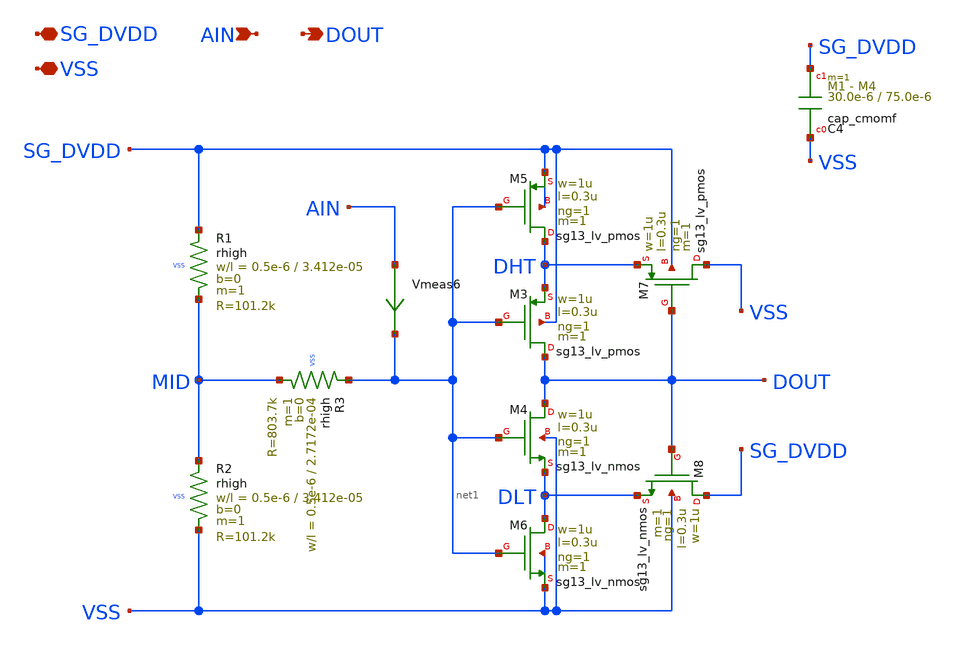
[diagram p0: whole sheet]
** sch_path: macros/schmitt_trigger_pullmid/schematic/xschem/schmitt_trigger_pullmid.sch
**.subckt schmitt_trigger_pullmid SG_DVDD VSS AIN DOUT
*.iopin SG_DVDD
*.iopin VSS
*.ipin AIN
*.opin DOUT
Vmeas6 AIN net1 0
.save i(vmeas6)
XR1 SG_DVDD MID VSS rhigh w=0.5e-6 l=3.412e-05 m=1 b=0 mm_ok=1
XR2 MID VSS VSS rhigh w=0.5e-6 l=3.412e-05 m=1 b=0 mm_ok=1
XR3 net1 MID VSS rhigh w=0.5e-6 l=2.7172e-04 m=1 b=0 mm_ok=1
XC4 VSS SG_DVDD cap_cmomf w=30.0e-6 l=75.0e-6 mmin=1 mmax=4 subblock=0 rfmodel=0 subscale=1 m=1
+ mm_ok=1
XM4 DOUT net1 DLT VSS sg13_lv_nmos w=1u l=0.3u ng=1 m=1 mm_ok=1
XM5 DHT net1 SG_DVDD SG_DVDD sg13_lv_pmos w=1u l=0.3u ng=1 m=1 mm_ok=1
XM3 DOUT net1 DHT SG_DVDD sg13_lv_pmos w=1u l=0.3u ng=1 m=1 mm_ok=1
XM7 VSS DOUT DHT SG_DVDD sg13_lv_pmos w=1u l=0.3u ng=1 m=1 mm_ok=1
XM6 DLT net1 VSS VSS sg13_lv_nmos w=1u l=0.3u ng=1 m=1 mm_ok=1
XM8 SG_DVDD DOUT DLT VSS sg13_lv_nmos w=1u l=0.3u ng=1 m=1 mm_ok=1
**.ends
.end
